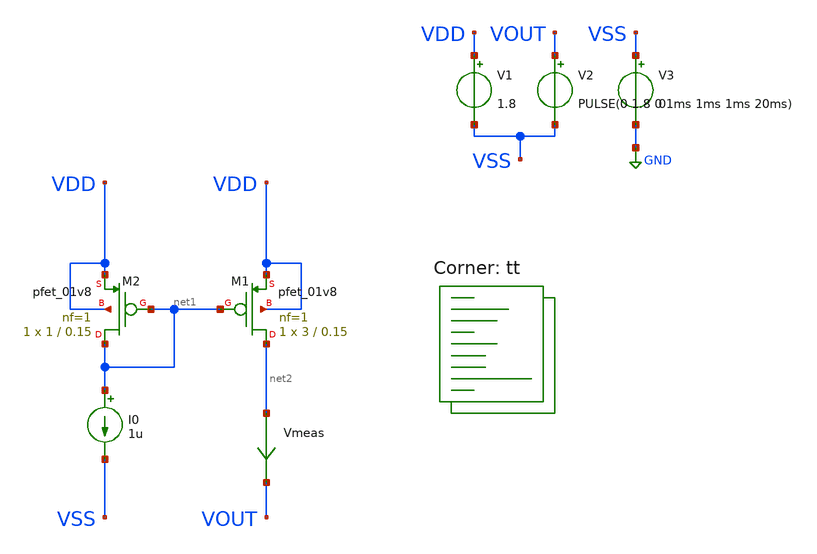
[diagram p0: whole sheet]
** sch_path: week02_current_diffpair/tugas4_basic_current_mirror/pmos-current-mirror.sch
**.subckt pmos-current-mirror
I0 net1 VSS 1u
V1 VDD VSS 1.8
V2 VOUT VSS PULSE(0 1.8 0 1ms 1ms 1ms 20ms)
V3 VSS GND 0
XM1 net2 net1 VDD VDD sky130_fd_pr__pfet_01v8 L=0.15 W=3 nf=1 ad='int((nf+1)/2) * W/nf * 0.29' as='int((nf+2)/2) * W/nf * 0.29'
+ pd='2*int((nf+1)/2) * (W/nf + 0.29)' ps='2*int((nf+2)/2) * (W/nf + 0.29)' nrd='0.29 / W' nrs='0.29 / W'
+ sa=0 sb=0 sd=0 mult=1 m=1
XM2 net1 net1 VDD VDD sky130_fd_pr__pfet_01v8 L=0.15 W=1 nf=1 ad='int((nf+1)/2) * W/nf * 0.29' as='int((nf+2)/2) * W/nf * 0.29'
+ pd='2*int((nf+1)/2) * (W/nf + 0.29)' ps='2*int((nf+2)/2) * (W/nf + 0.29)' nrd='0.29 / W' nrs='0.29 / W'
+ sa=0 sb=0 sd=0 mult=1 m=1
Vmeas net2 VOUT 0
.save i(vmeas)
**** begin user architecture code
.lib $::SKYWATER_MODELS/sky130.lib.spice tt



	.param Wm2=1u

.control
	tran 0.1u 100ms

	plot I(Vmeas)


saveall
.endc


**** end user architecture code
**.ends
.GLOBAL GND
.end
